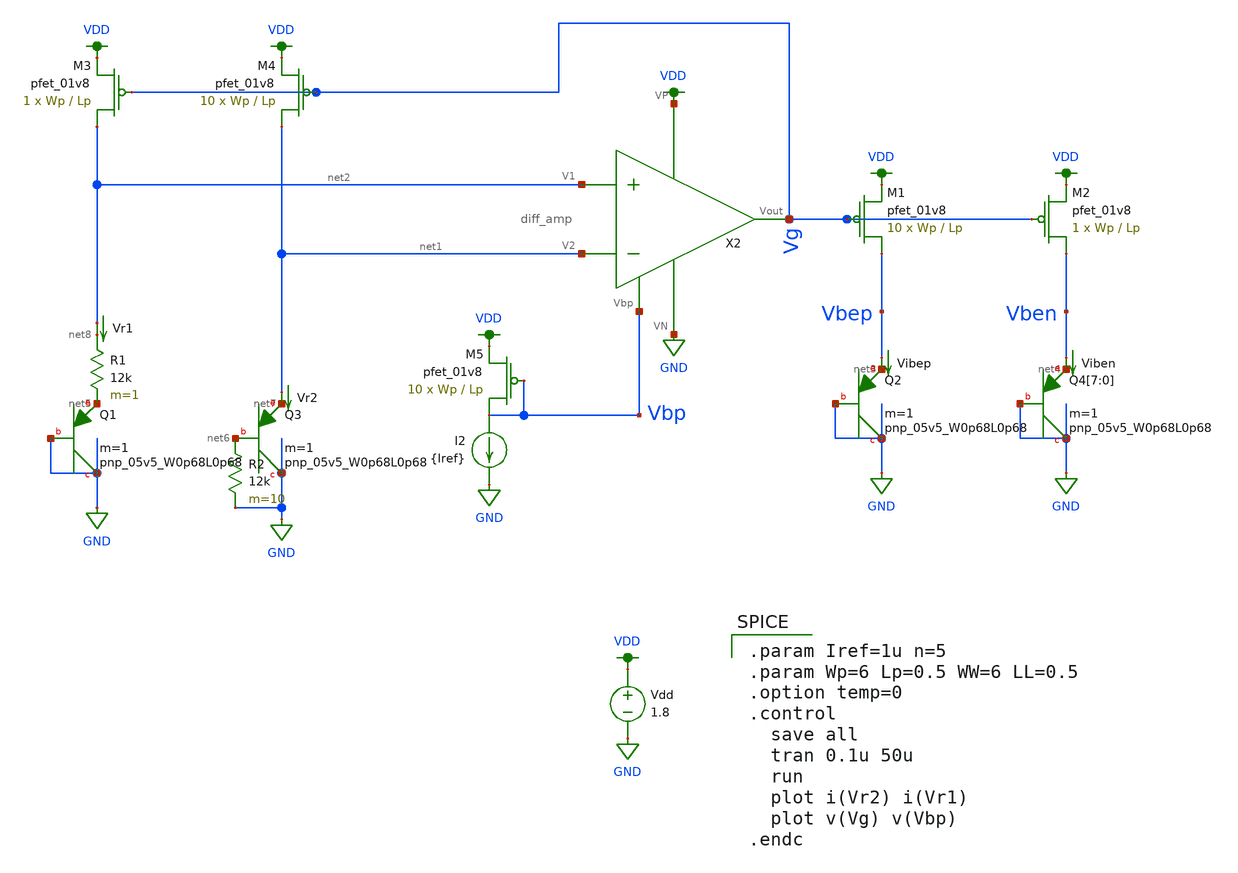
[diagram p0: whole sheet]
** sch_path: schematic/test/archive/bandgap_trantest.sch
**.subckt bandgap_trantest
XQ2 GND GND net3 sky130_fd_pr__pnp_05v5_W0p68L0p68 m=1
Vdd VDD GND 1.8
XM1 Vbep Vg VDD VDD sky130_fd_pr__pfet_01v8 L=Lp W=Wp nf=1 ad='int((nf+1)/2) * W/nf * 0.29' as='int((nf+2)/2) * W/nf * 0.29'
+ pd='2*int((nf+1)/2) * (W/nf + 0.29)' ps='2*int((nf+2)/2) * (W/nf + 0.29)' nrd='0.29 / W' nrs='0.29 / W'
+ sa=0 sb=0 sd=0 mult=10 m=10
XM2 Vben Vg VDD VDD sky130_fd_pr__pfet_01v8 L=Lp W=Wp nf=1 ad='int((nf+1)/2) * W/nf * 0.29' as='int((nf+2)/2) * W/nf * 0.29'
+ pd='2*int((nf+1)/2) * (W/nf + 0.29)' ps='2*int((nf+2)/2) * (W/nf + 0.29)' nrd='0.29 / W' nrs='0.29 / W'
+ sa=0 sb=0 sd=0 mult=1 m=1
I2 Vbp GND {Iref}
XQ4[7] GND GND net4 sky130_fd_pr__pnp_05v5_W0p68L0p68 m=1
XQ4[6] GND GND net4 sky130_fd_pr__pnp_05v5_W0p68L0p68 m=1
XQ4[5] GND GND net4 sky130_fd_pr__pnp_05v5_W0p68L0p68 m=1
XQ4[4] GND GND net4 sky130_fd_pr__pnp_05v5_W0p68L0p68 m=1
XQ4[3] GND GND net4 sky130_fd_pr__pnp_05v5_W0p68L0p68 m=1
XQ4[2] GND GND net4 sky130_fd_pr__pnp_05v5_W0p68L0p68 m=1
XQ4[1] GND GND net4 sky130_fd_pr__pnp_05v5_W0p68L0p68 m=1
XQ4[0] GND GND net4 sky130_fd_pr__pnp_05v5_W0p68L0p68 m=1
X2 VDD Vbp Vg net2 net1 GND diff_amp
XQ1 GND GND net5 sky130_fd_pr__pnp_05v5_W0p68L0p68 m=1
XQ3 GND net6 net7 sky130_fd_pr__pnp_05v5_W0p68L0p68 m=1
R1 net8 net5 12k m=1
R2 net6 GND 12k m=10
XM3 net2 Vg VDD VDD sky130_fd_pr__pfet_01v8 L=Lp W=Wp nf=1 ad='int((nf+1)/2) * W/nf * 0.29' as='int((nf+2)/2) * W/nf * 0.29'
+ pd='2*int((nf+1)/2) * (W/nf + 0.29)' ps='2*int((nf+2)/2) * (W/nf + 0.29)' nrd='0.29 / W' nrs='0.29 / W'
+ sa=0 sb=0 sd=0 mult=1 m=1
XM4 net1 Vg VDD VDD sky130_fd_pr__pfet_01v8 L=Lp W=Wp nf=1 ad='int((nf+1)/2) * W/nf * 0.29' as='int((nf+2)/2) * W/nf * 0.29'
+ pd='2*int((nf+1)/2) * (W/nf + 0.29)' ps='2*int((nf+2)/2) * (W/nf + 0.29)' nrd='0.29 / W' nrs='0.29 / W'
+ sa=0 sb=0 sd=0 mult=10 m=10
Vr1 net2 net8 0
.save i(vr1)
Vr2 net1 net7 0
.save i(vr2)
Vibep Vbep net3 0
.save i(vibep)
Viben Vben net4 0
.save i(viben)
XM5 Vbp Vbp VDD VDD sky130_fd_pr__pfet_01v8 L=Lp W=Wp nf=1 ad='int((nf+1)/2) * W/nf * 0.29' as='int((nf+2)/2) * W/nf * 0.29'
+ pd='2*int((nf+1)/2) * (W/nf + 0.29)' ps='2*int((nf+2)/2) * (W/nf + 0.29)' nrd='0.29 / W' nrs='0.29 / W'
+ sa=0 sb=0 sd=0 mult=10 m=10
**** begin user architecture code

.option wnflag=1
.param MC_SWITCH=0.0
.lib skywater/skywater-pdk/libraries/sky130_fd_pr_ngspice/latest/models/sky130.lib.spice tt


.param Iref=1u n=5
.param Wp=6 Lp=0.5 WW=6 LL=0.5
.option temp=0
.control
  save all
  tran 0.1u 50u
  run
  plot i(Vr2) i(Vr1)
  plot v(Vg) v(Vbp)
.endc

**** end user architecture code
**.ends
.GLOBAL GND
.GLOBAL VDD
.end
